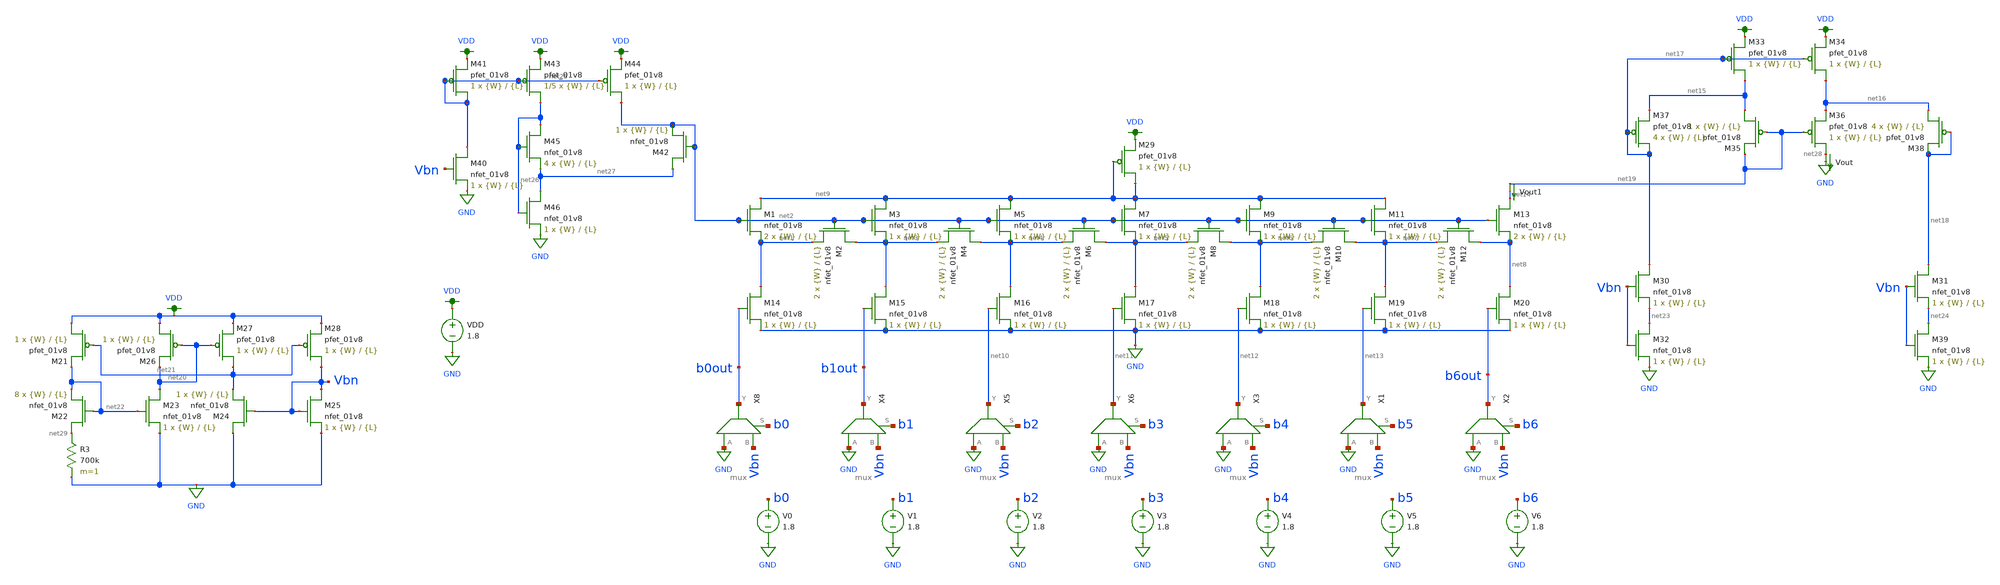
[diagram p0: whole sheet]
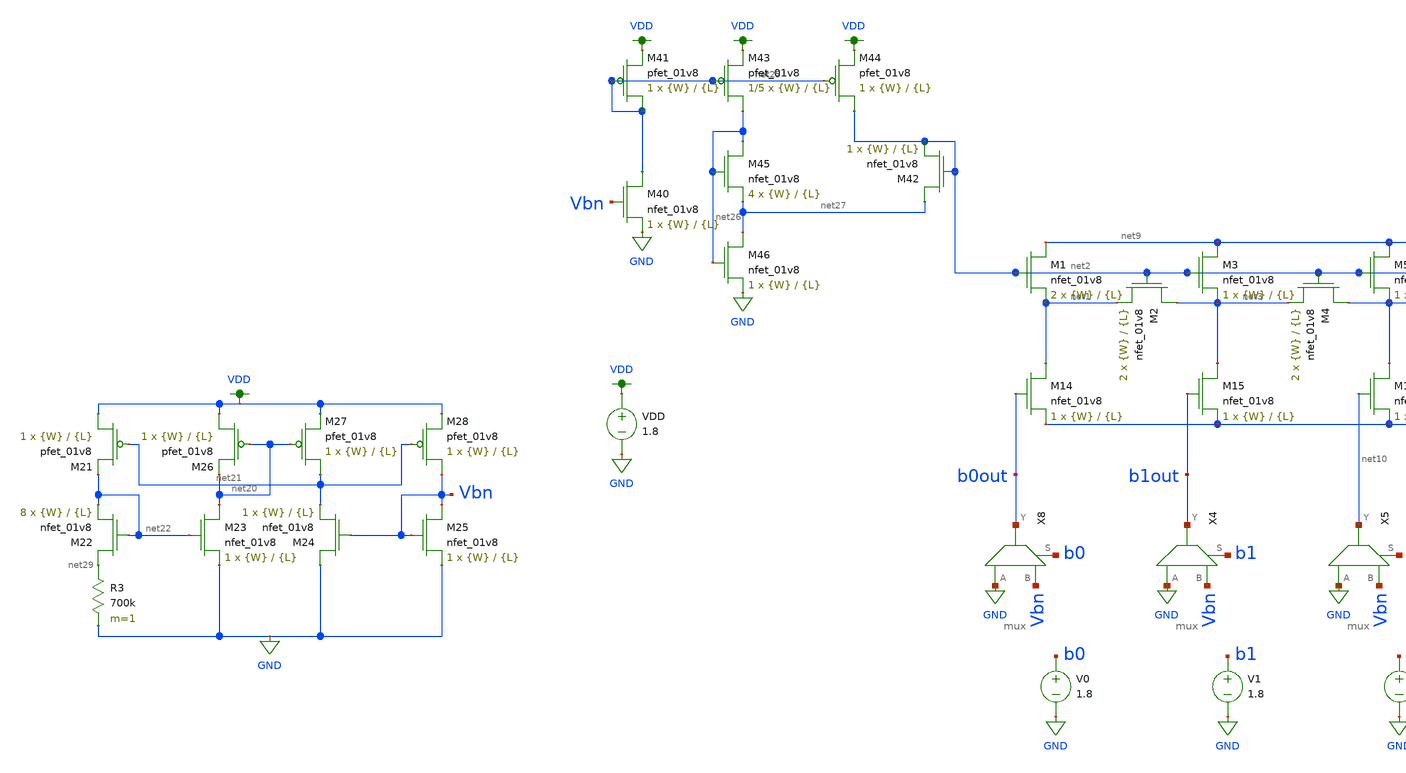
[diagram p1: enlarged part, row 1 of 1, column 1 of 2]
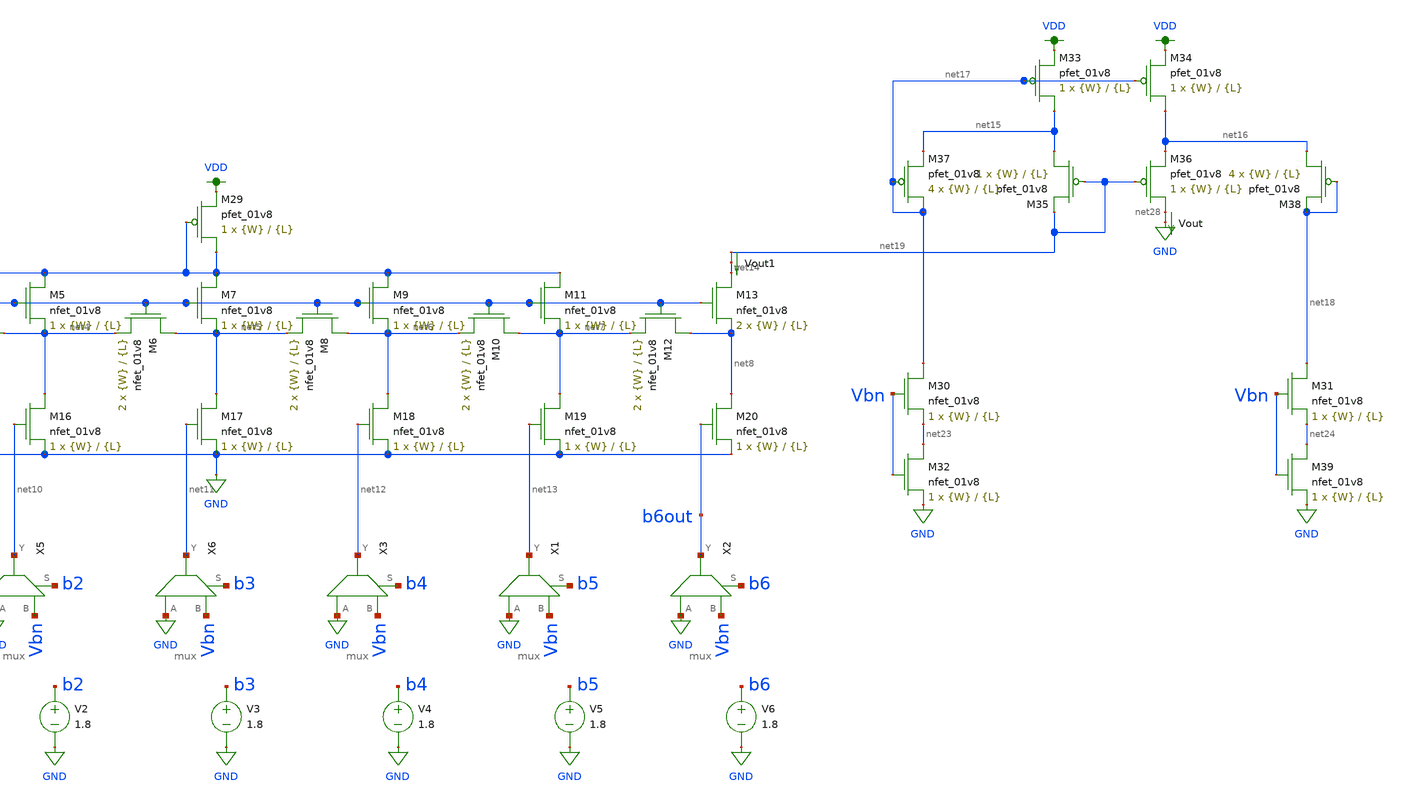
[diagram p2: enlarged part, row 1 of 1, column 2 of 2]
** sch_path: dac/schematics/monte_carlo_sim.sch
**.subckt monte_carlo_sim
XM1 net9 net2 net1 GND sky130_fd_pr__nfet_01v8 L={L} W={W} nf=1 ad='int((nf+1)/2) * W/nf * 0.29' as='int((nf+2)/2) * W/nf * 0.29'
+ pd='2*int((nf+1)/2) * (W/nf + 0.29)' ps='2*int((nf+2)/2) * (W/nf + 0.29)' nrd='0.29 / W' nrs='0.29 / W'
+ sa=0 sb=0 sd=0 mult=2 m=2
XM2 net3 net2 net1 GND sky130_fd_pr__nfet_01v8 L={L} W={W} nf=1 ad='int((nf+1)/2) * W/nf * 0.29' as='int((nf+2)/2) * W/nf * 0.29'
+ pd='2*int((nf+1)/2) * (W/nf + 0.29)' ps='2*int((nf+2)/2) * (W/nf + 0.29)' nrd='0.29 / W' nrs='0.29 / W'
+ sa=0 sb=0 sd=0 mult=2 m=2
XM3 net9 net2 net3 GND sky130_fd_pr__nfet_01v8 L={L} W={W} nf=1 ad='int((nf+1)/2) * W/nf * 0.29' as='int((nf+2)/2) * W/nf * 0.29'
+ pd='2*int((nf+1)/2) * (W/nf + 0.29)' ps='2*int((nf+2)/2) * (W/nf + 0.29)' nrd='0.29 / W' nrs='0.29 / W'
+ sa=0 sb=0 sd=0 mult=1 m=1
XM4 net4 net2 net3 GND sky130_fd_pr__nfet_01v8 L={L} W={W} nf=1 ad='int((nf+1)/2) * W/nf * 0.29' as='int((nf+2)/2) * W/nf * 0.29'
+ pd='2*int((nf+1)/2) * (W/nf + 0.29)' ps='2*int((nf+2)/2) * (W/nf + 0.29)' nrd='0.29 / W' nrs='0.29 / W'
+ sa=0 sb=0 sd=0 mult=2 m=2
XM5 net9 net2 net4 GND sky130_fd_pr__nfet_01v8 L={L} W={W} nf=1 ad='int((nf+1)/2) * W/nf * 0.29' as='int((nf+2)/2) * W/nf * 0.29'
+ pd='2*int((nf+1)/2) * (W/nf + 0.29)' ps='2*int((nf+2)/2) * (W/nf + 0.29)' nrd='0.29 / W' nrs='0.29 / W'
+ sa=0 sb=0 sd=0 mult=1 m=1
XM6 net5 net2 net4 GND sky130_fd_pr__nfet_01v8 L={L} W={W} nf=1 ad='int((nf+1)/2) * W/nf * 0.29' as='int((nf+2)/2) * W/nf * 0.29'
+ pd='2*int((nf+1)/2) * (W/nf + 0.29)' ps='2*int((nf+2)/2) * (W/nf + 0.29)' nrd='0.29 / W' nrs='0.29 / W'
+ sa=0 sb=0 sd=0 mult=2 m=2
XM7 net9 net2 net5 GND sky130_fd_pr__nfet_01v8 L={L} W={W} nf=1 ad='int((nf+1)/2) * W/nf * 0.29' as='int((nf+2)/2) * W/nf * 0.29'
+ pd='2*int((nf+1)/2) * (W/nf + 0.29)' ps='2*int((nf+2)/2) * (W/nf + 0.29)' nrd='0.29 / W' nrs='0.29 / W'
+ sa=0 sb=0 sd=0 mult=1 m=1
XM8 net6 net2 net5 GND sky130_fd_pr__nfet_01v8 L={L} W={W} nf=1 ad='int((nf+1)/2) * W/nf * 0.29' as='int((nf+2)/2) * W/nf * 0.29'
+ pd='2*int((nf+1)/2) * (W/nf + 0.29)' ps='2*int((nf+2)/2) * (W/nf + 0.29)' nrd='0.29 / W' nrs='0.29 / W'
+ sa=0 sb=0 sd=0 mult=2 m=2
XM9 net9 net2 net6 GND sky130_fd_pr__nfet_01v8 L={L} W={W} nf=1 ad='int((nf+1)/2) * W/nf * 0.29' as='int((nf+2)/2) * W/nf * 0.29'
+ pd='2*int((nf+1)/2) * (W/nf + 0.29)' ps='2*int((nf+2)/2) * (W/nf + 0.29)' nrd='0.29 / W' nrs='0.29 / W'
+ sa=0 sb=0 sd=0 mult=1 m=1
XM10 net7 net2 net6 GND sky130_fd_pr__nfet_01v8 L={L} W={W} nf=1 ad='int((nf+1)/2) * W/nf * 0.29' as='int((nf+2)/2) * W/nf * 0.29'
+ pd='2*int((nf+1)/2) * (W/nf + 0.29)' ps='2*int((nf+2)/2) * (W/nf + 0.29)' nrd='0.29 / W' nrs='0.29 / W'
+ sa=0 sb=0 sd=0 mult=2 m=2
XM11 net9 net2 net7 GND sky130_fd_pr__nfet_01v8 L={L} W={W} nf=1 ad='int((nf+1)/2) * W/nf * 0.29' as='int((nf+2)/2) * W/nf * 0.29'
+ pd='2*int((nf+1)/2) * (W/nf + 0.29)' ps='2*int((nf+2)/2) * (W/nf + 0.29)' nrd='0.29 / W' nrs='0.29 / W'
+ sa=0 sb=0 sd=0 mult=1 m=1
XM12 net8 net2 net7 GND sky130_fd_pr__nfet_01v8 L={L} W={W} nf=1 ad='int((nf+1)/2) * W/nf * 0.29' as='int((nf+2)/2) * W/nf * 0.29'
+ pd='2*int((nf+1)/2) * (W/nf + 0.29)' ps='2*int((nf+2)/2) * (W/nf + 0.29)' nrd='0.29 / W' nrs='0.29 / W'
+ sa=0 sb=0 sd=0 mult=2 m=2
XM13 net14 net2 net8 GND sky130_fd_pr__nfet_01v8 L={L} W={W} nf=1 ad='int((nf+1)/2) * W/nf * 0.29' as='int((nf+2)/2) * W/nf * 0.29'
+ pd='2*int((nf+1)/2) * (W/nf + 0.29)' ps='2*int((nf+2)/2) * (W/nf + 0.29)' nrd='0.29 / W' nrs='0.29 / W'
+ sa=0 sb=0 sd=0 mult=2 m=2
XM14 net1 b0out GND GND sky130_fd_pr__nfet_01v8 L={L} W={W} nf=1 ad='int((nf+1)/2) * W/nf * 0.29' as='int((nf+2)/2) * W/nf * 0.29'
+ pd='2*int((nf+1)/2) * (W/nf + 0.29)' ps='2*int((nf+2)/2) * (W/nf + 0.29)' nrd='0.29 / W' nrs='0.29 / W'
+ sa=0 sb=0 sd=0 mult=1 m=1
XM15 net3 b1out GND GND sky130_fd_pr__nfet_01v8 L={L} W={W} nf=1 ad='int((nf+1)/2) * W/nf * 0.29' as='int((nf+2)/2) * W/nf * 0.29'
+ pd='2*int((nf+1)/2) * (W/nf + 0.29)' ps='2*int((nf+2)/2) * (W/nf + 0.29)' nrd='0.29 / W' nrs='0.29 / W'
+ sa=0 sb=0 sd=0 mult=1 m=1
XM16 net4 net10 GND GND sky130_fd_pr__nfet_01v8 L={L} W={W} nf=1 ad='int((nf+1)/2) * W/nf * 0.29' as='int((nf+2)/2) * W/nf * 0.29'
+ pd='2*int((nf+1)/2) * (W/nf + 0.29)' ps='2*int((nf+2)/2) * (W/nf + 0.29)' nrd='0.29 / W' nrs='0.29 / W'
+ sa=0 sb=0 sd=0 mult=1 m=1
XM17 net5 net11 GND GND sky130_fd_pr__nfet_01v8 L={L} W={W} nf=1 ad='int((nf+1)/2) * W/nf * 0.29' as='int((nf+2)/2) * W/nf * 0.29'
+ pd='2*int((nf+1)/2) * (W/nf + 0.29)' ps='2*int((nf+2)/2) * (W/nf + 0.29)' nrd='0.29 / W' nrs='0.29 / W'
+ sa=0 sb=0 sd=0 mult=1 m=1
XM18 net6 net12 GND GND sky130_fd_pr__nfet_01v8 L={L} W={W} nf=1 ad='int((nf+1)/2) * W/nf * 0.29' as='int((nf+2)/2) * W/nf * 0.29'
+ pd='2*int((nf+1)/2) * (W/nf + 0.29)' ps='2*int((nf+2)/2) * (W/nf + 0.29)' nrd='0.29 / W' nrs='0.29 / W'
+ sa=0 sb=0 sd=0 mult=1 m=1
XM19 net7 net13 GND GND sky130_fd_pr__nfet_01v8 L={L} W={W} nf=1 ad='int((nf+1)/2) * W/nf * 0.29' as='int((nf+2)/2) * W/nf * 0.29'
+ pd='2*int((nf+1)/2) * (W/nf + 0.29)' ps='2*int((nf+2)/2) * (W/nf + 0.29)' nrd='0.29 / W' nrs='0.29 / W'
+ sa=0 sb=0 sd=0 mult=1 m=1
XM20 net8 b6out GND GND sky130_fd_pr__nfet_01v8 L={L} W={W} nf=1 ad='int((nf+1)/2) * W/nf * 0.29' as='int((nf+2)/2) * W/nf * 0.29'
+ pd='2*int((nf+1)/2) * (W/nf + 0.29)' ps='2*int((nf+2)/2) * (W/nf + 0.29)' nrd='0.29 / W' nrs='0.29 / W'
+ sa=0 sb=0 sd=0 mult=1 m=1
V0 b0 GND 1.8
V1 b1 GND 1.8
V2 b2 GND 1.8
V3 b3 GND 1.8
V4 b4 GND 1.8
V5 b5 GND 1.8
V6 b6 GND 1.8
Vout net28 GND 0
.save i(vout)
VDD VDD GND 1.8
XM33 net15 net17 VDD VDD sky130_fd_pr__pfet_01v8 L={L} W={W} nf=1 ad='int((nf+1)/2) * W/nf * 0.29' as='int((nf+2)/2) * W/nf * 0.29'
+ pd='2*int((nf+1)/2) * (W/nf + 0.29)' ps='2*int((nf+2)/2) * (W/nf + 0.29)' nrd='0.29 / W' nrs='0.29 / W'
+ sa=0 sb=0 sd=0 mult=1 m=1
XM34 net16 net17 VDD VDD sky130_fd_pr__pfet_01v8 L={L} W={W} nf=1 ad='int((nf+1)/2) * W/nf * 0.29' as='int((nf+2)/2) * W/nf * 0.29'
+ pd='2*int((nf+1)/2) * (W/nf + 0.29)' ps='2*int((nf+2)/2) * (W/nf + 0.29)' nrd='0.29 / W' nrs='0.29 / W'
+ sa=0 sb=0 sd=0 mult=1 m=1
XM35 net15 net19 net19 VDD sky130_fd_pr__pfet_01v8 L={L} W={W} nf=1 ad='int((nf+1)/2) * W/nf * 0.29'
+ as='int((nf+2)/2) * W/nf * 0.29' pd='2*int((nf+1)/2) * (W/nf + 0.29)' ps='2*int((nf+2)/2) * (W/nf + 0.29)'
+ nrd='0.29 / W' nrs='0.29 / W' sa=0 sb=0 sd=0 mult=1 m=1
XM36 net28 net19 net16 VDD sky130_fd_pr__pfet_01v8 L={L} W={W} nf=1 ad='int((nf+1)/2) * W/nf * 0.29'
+ as='int((nf+2)/2) * W/nf * 0.29' pd='2*int((nf+1)/2) * (W/nf + 0.29)' ps='2*int((nf+2)/2) * (W/nf + 0.29)'
+ nrd='0.29 / W' nrs='0.29 / W' sa=0 sb=0 sd=0 mult=1 m=1
XM37 net17 net17 net15 VDD sky130_fd_pr__pfet_01v8 L={L} W={W} nf=1 ad='int((nf+1)/2) * W/nf * 0.29'
+ as='int((nf+2)/2) * W/nf * 0.29' pd='2*int((nf+1)/2) * (W/nf + 0.29)' ps='2*int((nf+2)/2) * (W/nf + 0.29)'
+ nrd='0.29 / W' nrs='0.29 / W' sa=0 sb=0 sd=0 mult=4 m=4
XM38 net16 net18 net18 VDD sky130_fd_pr__pfet_01v8 L={L} W={W} nf=1 ad='int((nf+1)/2) * W/nf * 0.29'
+ as='int((nf+2)/2) * W/nf * 0.29' pd='2*int((nf+1)/2) * (W/nf + 0.29)' ps='2*int((nf+2)/2) * (W/nf + 0.29)'
+ nrd='0.29 / W' nrs='0.29 / W' sa=0 sb=0 sd=0 mult=4 m=4
XM21 VDD net21 net22 VDD sky130_fd_pr__pfet_01v8 L={L} W={W} nf=1 ad='int((nf+1)/2) * W/nf * 0.29' as='int((nf+2)/2) * W/nf * 0.29'
+ pd='2*int((nf+1)/2) * (W/nf + 0.29)' ps='2*int((nf+2)/2) * (W/nf + 0.29)' nrd='0.29 / W' nrs='0.29 / W'
+ sa=0 sb=0 sd=0 mult=1 m=1
XM22 net29 net22 net22 GND sky130_fd_pr__nfet_01v8 L={L} W={W} nf=1 ad='int((nf+1)/2) * W/nf * 0.29'
+ as='int((nf+2)/2) * W/nf * 0.29' pd='2*int((nf+1)/2) * (W/nf + 0.29)' ps='2*int((nf+2)/2) * (W/nf + 0.29)'
+ nrd='0.29 / W' nrs='0.29 / W' sa=0 sb=0 sd=0 mult=8 m=8
R3 net29 GND 700k m=1
XM23 net20 net22 GND GND sky130_fd_pr__nfet_01v8 L={L} W={W} nf=1 ad='int((nf+1)/2) * W/nf * 0.29' as='int((nf+2)/2) * W/nf * 0.29'
+ pd='2*int((nf+1)/2) * (W/nf + 0.29)' ps='2*int((nf+2)/2) * (W/nf + 0.29)' nrd='0.29 / W' nrs='0.29 / W'
+ sa=0 sb=0 sd=0 mult=1 m=1
XM24 GND Vbn net21 GND sky130_fd_pr__nfet_01v8 L={L} W={W} nf=1 ad='int((nf+1)/2) * W/nf * 0.29' as='int((nf+2)/2) * W/nf * 0.29'
+ pd='2*int((nf+1)/2) * (W/nf + 0.29)' ps='2*int((nf+2)/2) * (W/nf + 0.29)' nrd='0.29 / W' nrs='0.29 / W'
+ sa=0 sb=0 sd=0 mult=1 m=1
XM25 Vbn Vbn GND GND sky130_fd_pr__nfet_01v8 L={L} W={W} nf=1 ad='int((nf+1)/2) * W/nf * 0.29' as='int((nf+2)/2) * W/nf * 0.29'
+ pd='2*int((nf+1)/2) * (W/nf + 0.29)' ps='2*int((nf+2)/2) * (W/nf + 0.29)' nrd='0.29 / W' nrs='0.29 / W'
+ sa=0 sb=0 sd=0 mult=1 m=1
XM26 VDD net20 net20 VDD sky130_fd_pr__pfet_01v8 L={L} W={W} nf=1 ad='int((nf+1)/2) * W/nf * 0.29' as='int((nf+2)/2) * W/nf * 0.29'
+ pd='2*int((nf+1)/2) * (W/nf + 0.29)' ps='2*int((nf+2)/2) * (W/nf + 0.29)' nrd='0.29 / W' nrs='0.29 / W'
+ sa=0 sb=0 sd=0 mult=1 m=1
XM27 net21 net20 VDD VDD sky130_fd_pr__pfet_01v8 L={L} W={W} nf=1 ad='int((nf+1)/2) * W/nf * 0.29' as='int((nf+2)/2) * W/nf * 0.29'
+ pd='2*int((nf+1)/2) * (W/nf + 0.29)' ps='2*int((nf+2)/2) * (W/nf + 0.29)' nrd='0.29 / W' nrs='0.29 / W'
+ sa=0 sb=0 sd=0 mult=1 m=1
XM28 Vbn net21 VDD VDD sky130_fd_pr__pfet_01v8 L={L} W={W} nf=1 ad='int((nf+1)/2) * W/nf * 0.29' as='int((nf+2)/2) * W/nf * 0.29'
+ pd='2*int((nf+1)/2) * (W/nf + 0.29)' ps='2*int((nf+2)/2) * (W/nf + 0.29)' nrd='0.29 / W' nrs='0.29 / W'
+ sa=0 sb=0 sd=0 mult=1 m=1
XM29 net9 net9 VDD VDD sky130_fd_pr__pfet_01v8 L={L} W={W} nf=1 ad='int((nf+1)/2) * W/nf * 0.29' as='int((nf+2)/2) * W/nf * 0.29'
+ pd='2*int((nf+1)/2) * (W/nf + 0.29)' ps='2*int((nf+2)/2) * (W/nf + 0.29)' nrd='0.29 / W' nrs='0.29 / W'
+ sa=0 sb=0 sd=0 mult=1 m=1
XM30 net17 Vbn net23 GND sky130_fd_pr__nfet_01v8 L={L} W={W} nf=1 ad='int((nf+1)/2) * W/nf * 0.29' as='int((nf+2)/2) * W/nf * 0.29'
+ pd='2*int((nf+1)/2) * (W/nf + 0.29)' ps='2*int((nf+2)/2) * (W/nf + 0.29)' nrd='0.29 / W' nrs='0.29 / W'
+ sa=0 sb=0 sd=0 mult=1 m=1
XM31 net18 Vbn net24 GND sky130_fd_pr__nfet_01v8 L={L} W={W} nf=1 ad='int((nf+1)/2) * W/nf * 0.29' as='int((nf+2)/2) * W/nf * 0.29'
+ pd='2*int((nf+1)/2) * (W/nf + 0.29)' ps='2*int((nf+2)/2) * (W/nf + 0.29)' nrd='0.29 / W' nrs='0.29 / W'
+ sa=0 sb=0 sd=0 mult=1 m=1
XM32 net23 Vbn GND GND sky130_fd_pr__nfet_01v8 L={L} W={W} nf=1 ad='int((nf+1)/2) * W/nf * 0.29' as='int((nf+2)/2) * W/nf * 0.29'
+ pd='2*int((nf+1)/2) * (W/nf + 0.29)' ps='2*int((nf+2)/2) * (W/nf + 0.29)' nrd='0.29 / W' nrs='0.29 / W'
+ sa=0 sb=0 sd=0 mult=1 m=1
XM39 net24 Vbn GND GND sky130_fd_pr__nfet_01v8 L={L} W={W} nf=1 ad='int((nf+1)/2) * W/nf * 0.29' as='int((nf+2)/2) * W/nf * 0.29'
+ pd='2*int((nf+1)/2) * (W/nf + 0.29)' ps='2*int((nf+2)/2) * (W/nf + 0.29)' nrd='0.29 / W' nrs='0.29 / W'
+ sa=0 sb=0 sd=0 mult=1 m=1
X8 GND Vbn b0out b0 mux
X4 GND Vbn b1out b1 mux
X5 GND Vbn net10 b2 mux
X6 GND Vbn net11 b3 mux
X3 GND Vbn net12 b4 mux
X1 GND Vbn net13 b5 mux
X2 GND Vbn b6out b6 mux
Vout1 net19 net14 0
.save i(vout1)
XM40 net25 Vbn GND GND sky130_fd_pr__nfet_01v8 L={L} W={W} nf=1 ad='int((nf+1)/2) * W/nf * 0.29' as='int((nf+2)/2) * W/nf * 0.29'
+ pd='2*int((nf+1)/2) * (W/nf + 0.29)' ps='2*int((nf+2)/2) * (W/nf + 0.29)' nrd='0.29 / W' nrs='0.29 / W'
+ sa=0 sb=0 sd=0 mult=1 m=1
XM41 net25 net25 VDD VDD sky130_fd_pr__pfet_01v8 L={L} W={W} nf=1 ad='int((nf+1)/2) * W/nf * 0.29' as='int((nf+2)/2) * W/nf * 0.29'
+ pd='2*int((nf+1)/2) * (W/nf + 0.29)' ps='2*int((nf+2)/2) * (W/nf + 0.29)' nrd='0.29 / W' nrs='0.29 / W'
+ sa=0 sb=0 sd=0 mult=1 m=1
XM42 net27 net2 net2 GND sky130_fd_pr__nfet_01v8 L={L} W={W} nf=1 ad='int((nf+1)/2) * W/nf * 0.29' as='int((nf+2)/2) * W/nf * 0.29'
+ pd='2*int((nf+1)/2) * (W/nf + 0.29)' ps='2*int((nf+2)/2) * (W/nf + 0.29)' nrd='0.29 / W' nrs='0.29 / W'
+ sa=0 sb=0 sd=0 mult=1 m=1
XM43 net26 net25 VDD VDD sky130_fd_pr__pfet_01v8 L={L} W={W} nf=1 ad='int((nf+1)/2) * W/nf * 0.29' as='int((nf+2)/2) * W/nf * 0.29'
+ pd='2*int((nf+1)/2) * (W/nf + 0.29)' ps='2*int((nf+2)/2) * (W/nf + 0.29)' nrd='0.29 / W' nrs='0.29 / W'
+ sa=0 sb=0 sd=0 mult=1/5 m=1/5
XM44 net2 net25 VDD VDD sky130_fd_pr__pfet_01v8 L={L} W={W} nf=1 ad='int((nf+1)/2) * W/nf * 0.29' as='int((nf+2)/2) * W/nf * 0.29'
+ pd='2*int((nf+1)/2) * (W/nf + 0.29)' ps='2*int((nf+2)/2) * (W/nf + 0.29)' nrd='0.29 / W' nrs='0.29 / W'
+ sa=0 sb=0 sd=0 mult=1 m=1
XM45 net26 net26 net27 GND sky130_fd_pr__nfet_01v8 L={L} W={W} nf=1 ad='int((nf+1)/2) * W/nf * 0.29'
+ as='int((nf+2)/2) * W/nf * 0.29' pd='2*int((nf+1)/2) * (W/nf + 0.29)' ps='2*int((nf+2)/2) * (W/nf + 0.29)'
+ nrd='0.29 / W' nrs='0.29 / W' sa=0 sb=0 sd=0 mult=4 m=4
XM46 net27 net26 GND GND sky130_fd_pr__nfet_01v8 L={L} W={W} nf=1 ad='int((nf+1)/2) * W/nf * 0.29' as='int((nf+2)/2) * W/nf * 0.29'
+ pd='2*int((nf+1)/2) * (W/nf + 0.29)' ps='2*int((nf+2)/2) * (W/nf + 0.29)' nrd='0.29 / W' nrs='0.29 / W'
+ sa=0 sb=0 sd=0 mult=1 m=1
**** begin user architecture code

.param W=32
.param L=8
.control
  set wr_singlescale
  let runs = 2
  let run = 1
  while run <= runs
    set appendwrite = FALSE
    set wr_vecnames
    let code = 0
    while code < 128
      if code eq 0
        let b0 = 0
      else
        let b0 = code % 2 * 1.8
      end
      if floor(code / 2) eq 0
        let b1 = 0
      else
        let b1 = floor(code / 2) % 2 * 1.8
      end
      if floor(code / 4) eq 0
        let b2 = 0
      else
        let b2 = floor(code / 4) % 2 * 1.8
      end
      if floor(code / 8) eq 0
        let b3 = 0
      else
        let b3 = floor(code / 8) % 2 * 1.8
      end
      if floor(code / 16) eq 0
        let b4 = 0
      else
        let b4 = floor(code / 16) % 2 * 1.8
      end
      if floor(code / 32) eq 0
        let b5 = 0
      else
        let b5 = floor(code / 32) % 2 * 1.8
      end
      if floor(code / 64) eq 0
        let b6 = 0
      else
        let b6 = floor(code / 64) % 2 * 1.8
      end
      alter v0 $&b0
      alter v1 $&b1
      alter v2 $&b2
      alter v3 $&b3
      alter v4 $&b4
      alter v5 $&b5
      alter v6 $&b6
      save all
      op
      wrdata ~/Documents/current-output-dac-vlsi/simulations/{$&run}.txt v(Vbn) i(Vout) i(Vout1) v(b6)
+ v(b5) v(b4) v(b3) v(b2) v(b1) v(b0) v(b0out) v(b1out) v(b6out)
      if code eq 0
        set appendwrite
        set wr_vecnames = FALSE
      end
      let code = code + 1
    end
    reset
    let run = run + 1
  end
  quit
.endc


.option wnflag=1
.param MC_SWITCH=1.0
.lib ~/skywater/skywater-pdk/libraries/sky130_fd_pr_ngspice/latest/models/sky130.lib.spice tt

**** end user architecture code
**.ends

* expanding   symbol:  /home/madvlsi/Documents/current-output-dac-vlsi/schematics/mux.sym # of
*+ pins=4
** sym_path: dac/schematics/mux.sym
** sch_path: dac/schematics/mux.sch
.subckt mux A B Y S
*.ipin A
*.ipin B
*.ipin S
*.opin Y
XM1 A S Y VDD sky130_fd_pr__pfet_01v8 L=0.15 W=1 nf=1 ad='int((nf+1)/2) * W/nf * 0.29' as='int((nf+2)/2) * W/nf * 0.29'
+ pd='2*int((nf+1)/2) * (W/nf + 0.29)' ps='2*int((nf+2)/2) * (W/nf + 0.29)' nrd='0.29 / W' nrs='0.29 / W'
+ sa=0 sb=0 sd=0 mult=1 m=1
XM3 net1 S VDD VDD sky130_fd_pr__pfet_01v8 L=0.15 W=1 nf=1 ad='int((nf+1)/2) * W/nf * 0.29' as='int((nf+2)/2) * W/nf * 0.29'
+ pd='2*int((nf+1)/2) * (W/nf + 0.29)' ps='2*int((nf+2)/2) * (W/nf + 0.29)' nrd='0.29 / W' nrs='0.29 / W'
+ sa=0 sb=0 sd=0 mult=1 m=1
XM4 net1 S GND GND sky130_fd_pr__nfet_01v8 L=0.15 W=1 nf=1 ad='int((nf+1)/2) * W/nf * 0.29' as='int((nf+2)/2) * W/nf * 0.29'
+ pd='2*int((nf+1)/2) * (W/nf + 0.29)' ps='2*int((nf+2)/2) * (W/nf + 0.29)' nrd='0.29 / W' nrs='0.29 / W'
+ sa=0 sb=0 sd=0 mult=1 m=1
XM5 A net1 Y GND sky130_fd_pr__nfet_01v8 L=0.15 W=1 nf=1 ad='int((nf+1)/2) * W/nf * 0.29' as='int((nf+2)/2) * W/nf * 0.29'
+ pd='2*int((nf+1)/2) * (W/nf + 0.29)' ps='2*int((nf+2)/2) * (W/nf + 0.29)' nrd='0.29 / W' nrs='0.29 / W'
+ sa=0 sb=0 sd=0 mult=1 m=1
XM2 B net1 Y VDD sky130_fd_pr__pfet_01v8 L=0.15 W=1 nf=1 ad='int((nf+1)/2) * W/nf * 0.29' as='int((nf+2)/2) * W/nf * 0.29'
+ pd='2*int((nf+1)/2) * (W/nf + 0.29)' ps='2*int((nf+2)/2) * (W/nf + 0.29)' nrd='0.29 / W' nrs='0.29 / W'
+ sa=0 sb=0 sd=0 mult=1 m=1
XM6 B S Y GND sky130_fd_pr__nfet_01v8 L=0.15 W=1 nf=1 ad='int((nf+1)/2) * W/nf * 0.29' as='int((nf+2)/2) * W/nf * 0.29'
+ pd='2*int((nf+1)/2) * (W/nf + 0.29)' ps='2*int((nf+2)/2) * (W/nf + 0.29)' nrd='0.29 / W' nrs='0.29 / W'
+ sa=0 sb=0 sd=0 mult=1 m=1
.ends

.GLOBAL GND
.GLOBAL VDD
.end
